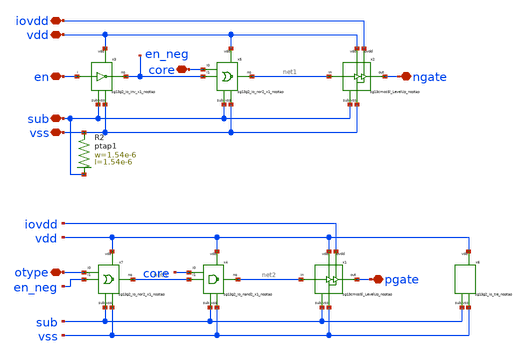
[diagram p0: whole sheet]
** sch_path: ihp-sg13cmos5l/libs.tech/xschem/hm_stdcells/hm_GateDecode_OpenDrain_noptap.sch
**.subckt hm_GateDecode_OpenDrain_noptap pgate ngate iovdd vss en vdd sub core otype
*.iopin pgate
*.iopin ngate
*.iopin iovdd
*.iopin vss
*.iopin en
*.iopin vdd
*.iopin sub
*.iopin core
*.iopin otype
x1 iovdd vss net2 pgate vdd sub sg13cmos5l_LevelUp_noptap
x2 iovdd vss net1 ngate vdd sub sg13cmos5l_LevelUp_noptap
x3 vss en en_neg vdd sub sg13g2_io_inv_x1_noptap
x4 vss core net2 vdd sub net3 sg13g2_io_nand2_x1_noptap
x5 vss core net1 vdd sub en_neg sg13g2_io_nor2_x1_noptap
x6 vss vdd sub sg13g2_io_tie_noptap
XR2 vss sub ptap1 R=114.9 w=1.54e-6 l=1.54e-6
x7 vss otype net3 vdd sub en_neg sg13g2_io_nor2_x1_noptap
**.ends
.end
